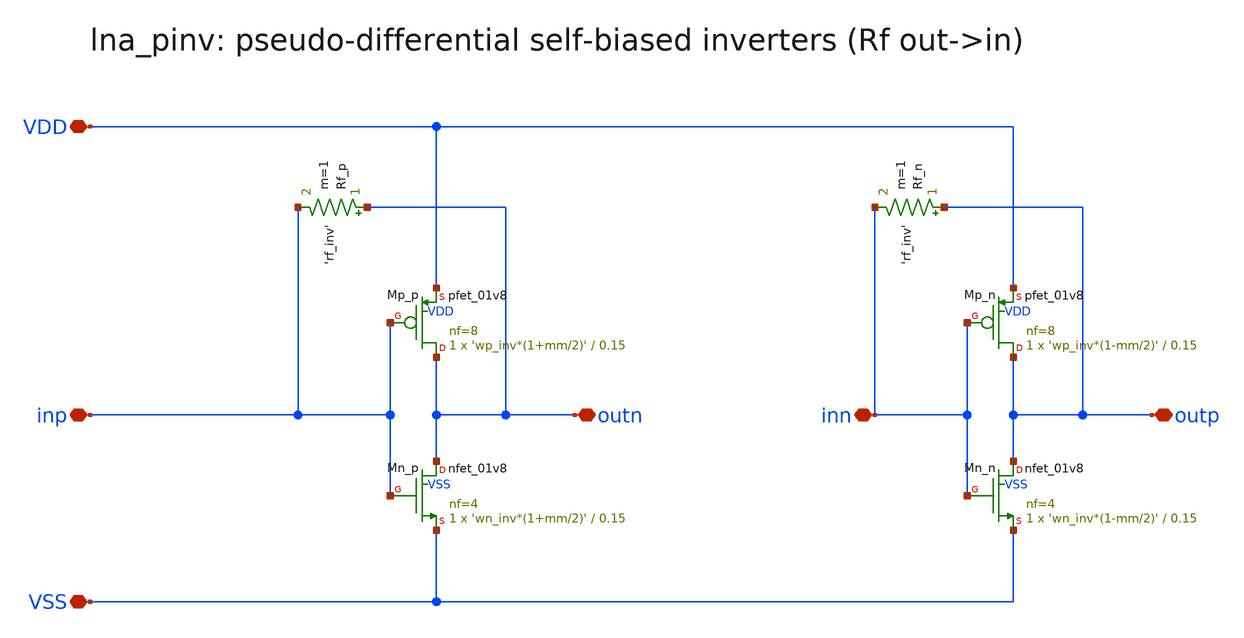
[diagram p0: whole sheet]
** sch_path: xschem/lna_pinv.sch
**.subckt lna_pinv VDD VSS inp inn outp outn
*.iopin VDD
*.iopin VSS
*.iopin inp
*.iopin inn
*.iopin outp
*.iopin outn
XMp_p outn inp VDD VDD sky130_fd_pr__pfet_01v8 L=0.15 W='wp_inv*(1+mm/2)' nf=8 ad='int((nf+1)/2) * W/nf * 0.29'
+ as='int((nf+2)/2) * W/nf * 0.29' pd='2*int((nf+1)/2) * (W/nf + 0.29)' ps='2*int((nf+2)/2) * (W/nf + 0.29)'
+ nrd='0.29 / W' nrs='0.29 / W' sa=0 sb=0 sd=0 mult=1 m=1
XMn_p outn inp VSS VSS sky130_fd_pr__nfet_01v8 L=0.15 W='wn_inv*(1+mm/2)' nf=4 ad='int((nf+1)/2) * W/nf * 0.29'
+ as='int((nf+2)/2) * W/nf * 0.29' pd='2*int((nf+1)/2) * (W/nf + 0.29)' ps='2*int((nf+2)/2) * (W/nf + 0.29)'
+ nrd='0.29 / W' nrs='0.29 / W' sa=0 sb=0 sd=0 mult=1 m=1
Rf_p outn inp 'rf_inv' m=1
XMp_n outp inn VDD VDD sky130_fd_pr__pfet_01v8 L=0.15 W='wp_inv*(1-mm/2)' nf=8 ad='int((nf+1)/2) * W/nf * 0.29'
+ as='int((nf+2)/2) * W/nf * 0.29' pd='2*int((nf+1)/2) * (W/nf + 0.29)' ps='2*int((nf+2)/2) * (W/nf + 0.29)'
+ nrd='0.29 / W' nrs='0.29 / W' sa=0 sb=0 sd=0 mult=1 m=1
XMn_n outp inn VSS VSS sky130_fd_pr__nfet_01v8 L=0.15 W='wn_inv*(1-mm/2)' nf=4 ad='int((nf+1)/2) * W/nf * 0.29'
+ as='int((nf+2)/2) * W/nf * 0.29' pd='2*int((nf+1)/2) * (W/nf + 0.29)' ps='2*int((nf+2)/2) * (W/nf + 0.29)'
+ nrd='0.29 / W' nrs='0.29 / W' sa=0 sb=0 sd=0 mult=1 m=1
Rf_n outp inn 'rf_inv' m=1
**.ends
.end
